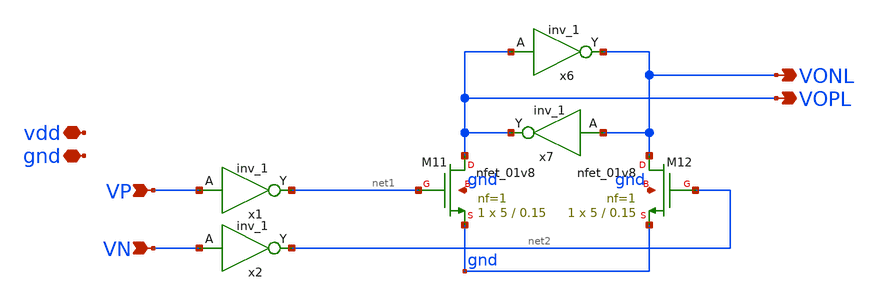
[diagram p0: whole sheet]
** sch_path: xschem/adc_strongarm_latch.sch
**.subckt adc_strongarm_latch vdd gnd VP VN VOPL VONL
*.iopin vdd
*.iopin gnd
*.ipin VP
*.ipin VN
*.opin VOPL
*.opin VONL
XM11 VOPL net1 gnd gnd sky130_fd_pr__nfet_01v8 L=0.15 W=5 nf=1 ad='int((nf+1)/2) * W/nf * 0.29' as='int((nf+2)/2) * W/nf * 0.29'
+ pd='2*int((nf+1)/2) * (W/nf + 0.29)' ps='2*int((nf+2)/2) * (W/nf + 0.29)' nrd='0.29 / W' nrs='0.29 / W'
+ sa=0 sb=0 sd=0 mult=1 m=1
XM12 VONL net2 gnd gnd sky130_fd_pr__nfet_01v8 L=0.15 W=5 nf=1 ad='int((nf+1)/2) * W/nf * 0.29' as='int((nf+2)/2) * W/nf * 0.29'
+ pd='2*int((nf+1)/2) * (W/nf + 0.29)' ps='2*int((nf+2)/2) * (W/nf + 0.29)' nrd='0.29 / W' nrs='0.29 / W'
+ sa=0 sb=0 sd=0 mult=1 m=1
x6 VOPL gnd gnd vdd vdd VONL sky130_fd_sc_hs__inv_1
x7 VONL gnd gnd vdd vdd VOPL sky130_fd_sc_hs__inv_1
x1 VP gnd gnd vdd vdd net1 sky130_fd_sc_hs__inv_1
x2 VN gnd gnd vdd vdd net2 sky130_fd_sc_hs__inv_1
**.ends
.end
